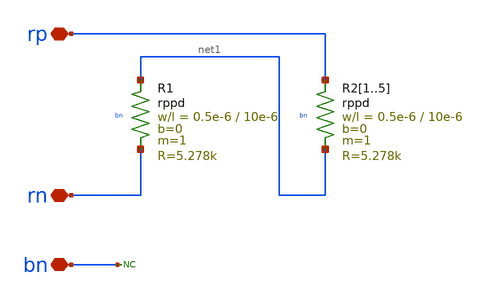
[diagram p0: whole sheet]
** sch_path: xschem/bandgap_simple_res-6k.sch
* (c) 2025 H. Pretl, Apache-2.0 license
**.subckt bandgap_simple_res-6k rp rn bn
*.iopin rp
*.iopin rn
*.iopin bn
XR1 net1 rn bn rppd w=0.5e-6 l=10e-6 m=1 b=0 mm_ok=1
XR21 rp net1 bn rppd w=0.5e-6 l=10e-6 m=1 b=0 mm_ok=1
XR22 rp net1 bn rppd w=0.5e-6 l=10e-6 m=1 b=0 mm_ok=1
XR23 rp net1 bn rppd w=0.5e-6 l=10e-6 m=1 b=0 mm_ok=1
XR24 rp net1 bn rppd w=0.5e-6 l=10e-6 m=1 b=0 mm_ok=1
XR25 rp net1 bn rppd w=0.5e-6 l=10e-6 m=1 b=0 mm_ok=1
* noconn bn
**.ends
.end
